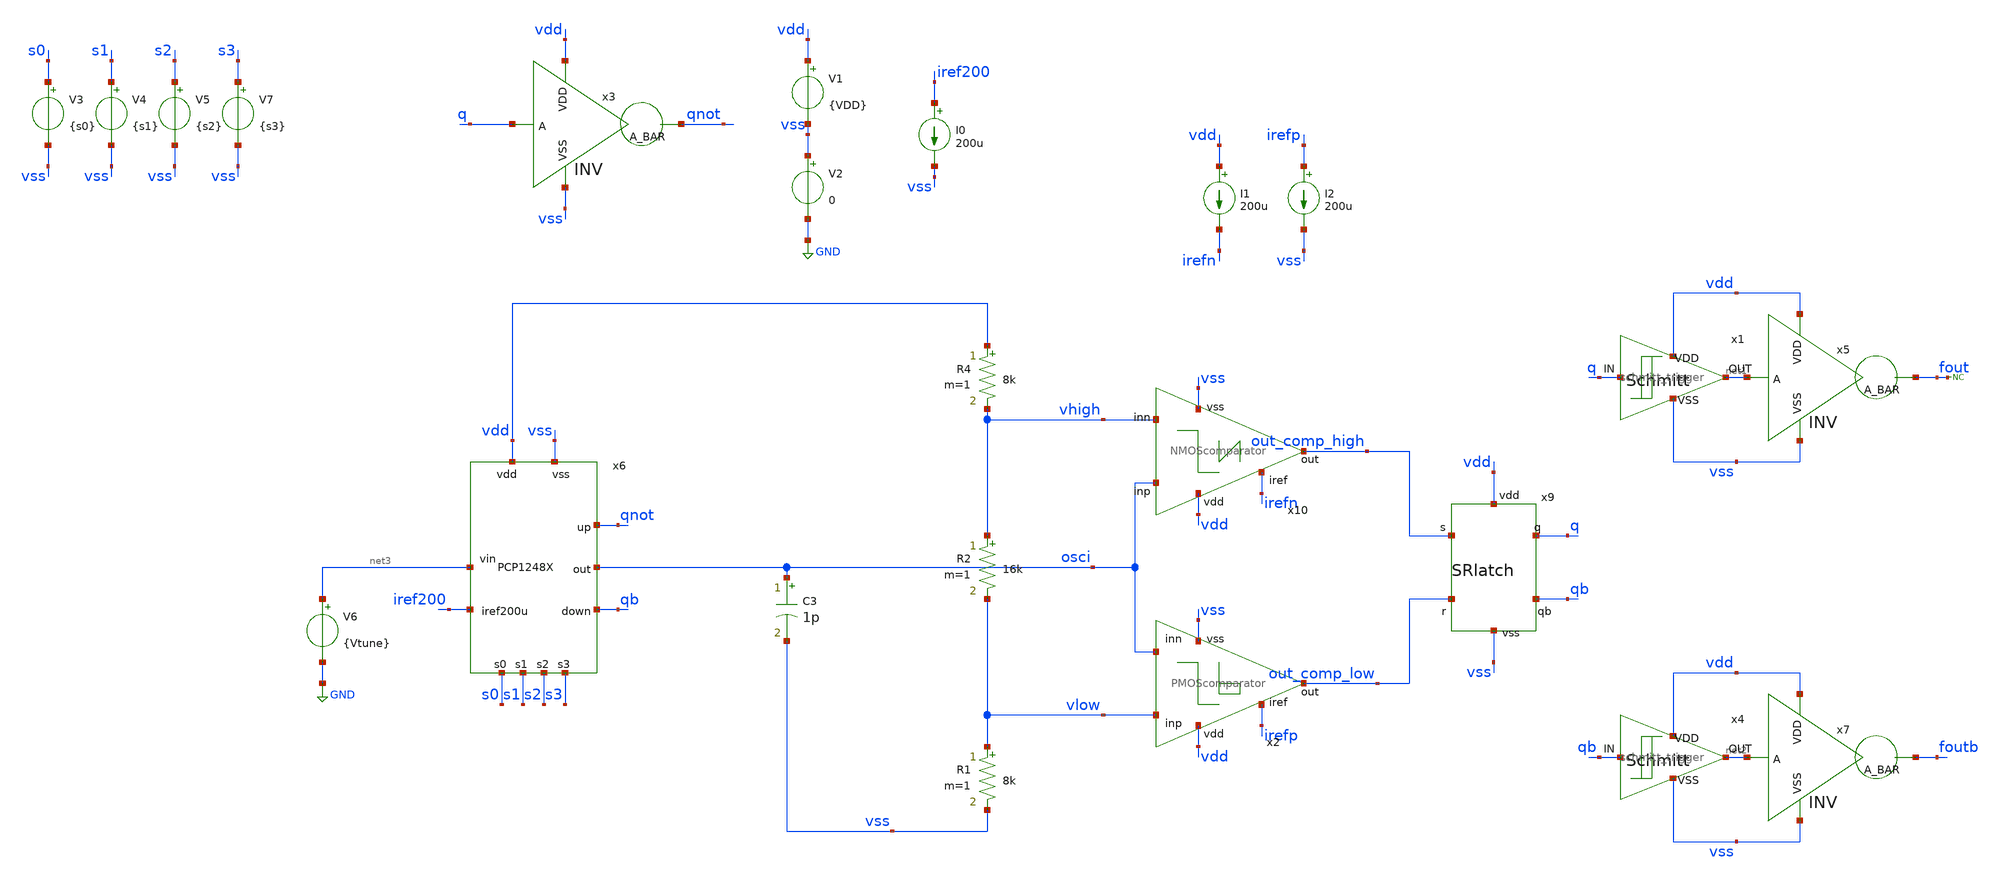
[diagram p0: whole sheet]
** sch_path: designs/libs/qw_core_analog/VCO0907/VCO0907.sch
**.subckt VCO0907
V1 vdd vss {VDD}
V2 vss GND 0
I1 vdd irefn 200u
I2 irefp vss 200u
R1 vlow vss 8k m=1
R2 vhigh vlow 16k m=1
R4 vdd vhigh 8k m=1
x9 vdd out_comp_high q qb out_comp_low vss SRlatch
x2 vdd irefp vlow out_comp_low osci vss PMOScomparator
x10 vdd osci out_comp_high vhigh irefn vss NMOScomparator
x3 vdd q qnot vss INV
x1 q net1 vdd vss schmitt_trigger
x4 qb net2 vdd vss schmitt_trigger
x5 vdd net1 fout vss INV
x7 vdd net2 foutb vss INV
V6 net3 GND {Vtune}
I0 iref200 vss 200u
* noconn fout
V3 s0 vss {s0}
V4 s1 vss {s1}
V5 s2 vss {s2}
C3 osci vss 1p m=1
x6 vdd vss net3 iref200 osci qnot qb s0 s1 s2 s3 PCP1248X
V7 s3 vss {s3}
**** begin user architecture code



.param VDD = 3.3
.param Vtune = 2
.param s0 = 3.3 s1 = 0 s2 = 0 s3 = 0
.param VIN=1
*V6 net3 0 {Vtune}
.meas tran period1 TRIG v(fout) VAL=1.65 RISE=15 TARG v(fout) VAL=1.65 RISE=16
.meas tran freq param='1/period1'

.control
save all

let vstart = 0.0
let vstop = 3.3
let vstep = 0.1

foreach VINVAL 2.0
    alterparam Vtune = $VINVAL
    reset
    tran 10p 2u
end

write VCO0907.raw
.endc



.include $::180MCU_MODELS/design.ngspice
.lib $::180MCU_MODELS/sm141064.ngspice typical
.lib $::180MCU_MODELS/sm141064.ngspice cap_mim
.lib $::180MCU_MODELS/sm141064.ngspice res_typical
.lib $::180MCU_MODELS/sm141064.ngspice moscap_typical
.lib $::180MCU_MODELS/sm141064.ngspice mimcap_typical
* .lib $::180MCU_MODELS/sm141064.ngspice res_statistical

**** end user architecture code
**.ends
.GLOBAL GND
.end
